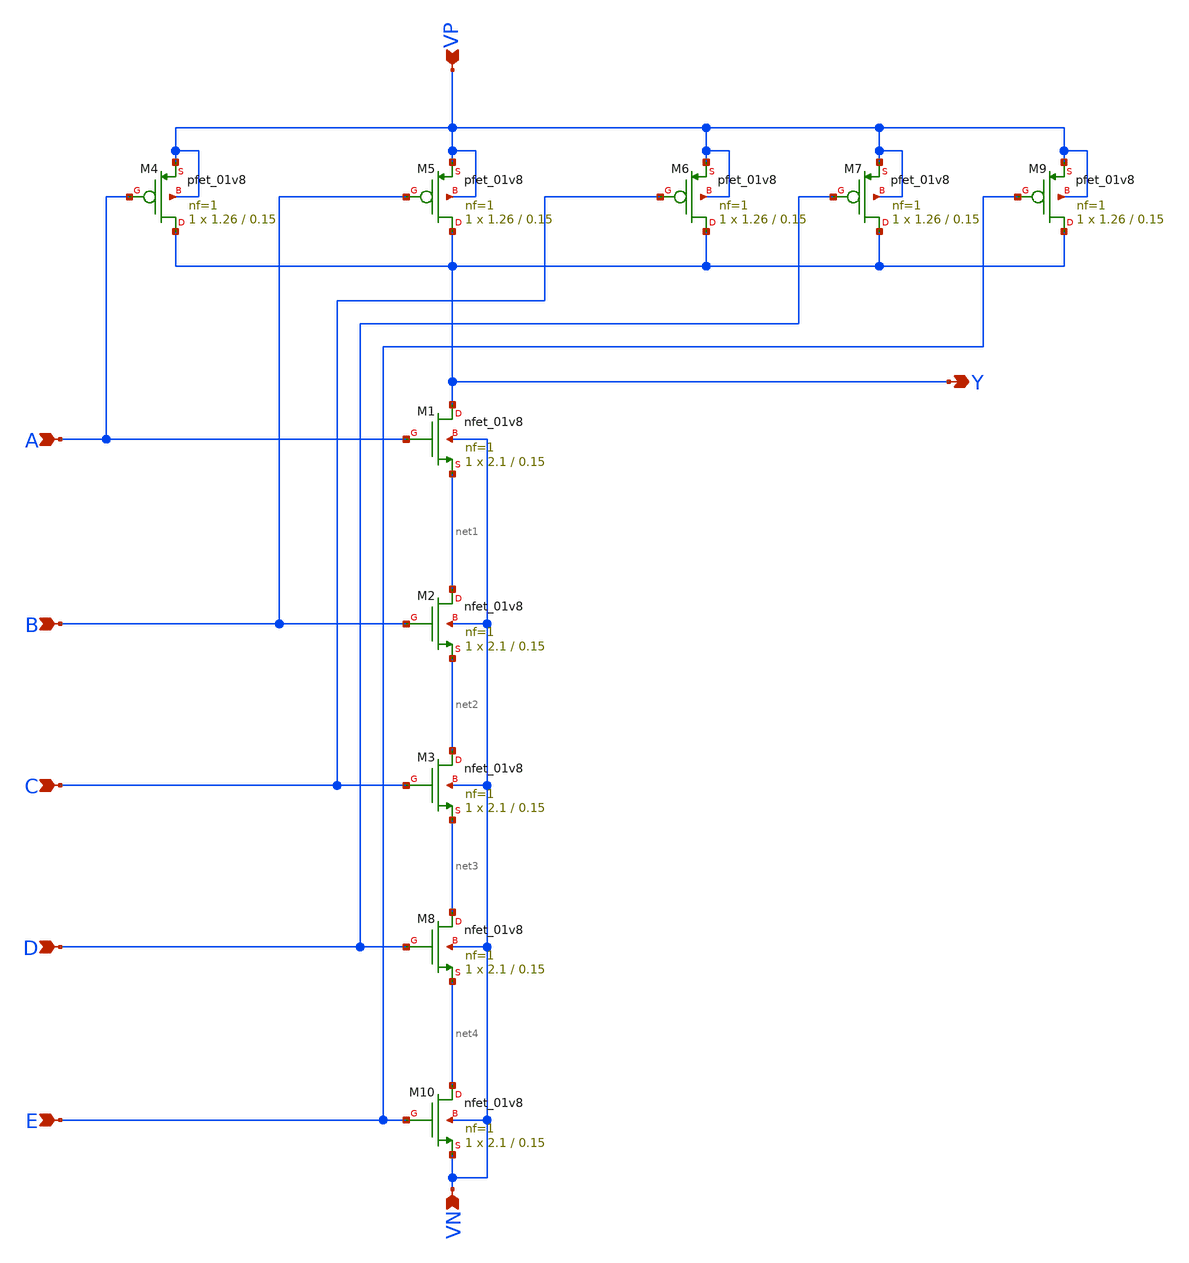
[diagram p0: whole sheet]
** sch_path: component/NAND5/nand5.sch
**.subckt nand5 A B C Y D E VN VP
*.ipin A
*.ipin B
*.ipin C
*.opin Y
*.ipin D
*.ipin E
*.ipin VN
*.ipin VP
XM1 Y A net1 VN sky130_fd_pr__nfet_01v8 L=0.15 W=2.1 nf=1 ad='int((nf+1)/2) * W/nf * 0.29' as='int((nf+2)/2) * W/nf * 0.29'
+ pd='2*int((nf+1)/2) * (W/nf + 0.29)' ps='2*int((nf+2)/2) * (W/nf + 0.29)' nrd='0.29 / W' nrs='0.29 / W'
+ sa=0 sb=0 sd=0 mult=1 m=1
XM2 net1 B net2 VN sky130_fd_pr__nfet_01v8 L=0.15 W=2.1 nf=1 ad='int((nf+1)/2) * W/nf * 0.29' as='int((nf+2)/2) * W/nf * 0.29'
+ pd='2*int((nf+1)/2) * (W/nf + 0.29)' ps='2*int((nf+2)/2) * (W/nf + 0.29)' nrd='0.29 / W' nrs='0.29 / W'
+ sa=0 sb=0 sd=0 mult=1 m=1
XM3 net2 C net3 VN sky130_fd_pr__nfet_01v8 L=0.15 W=2.1 nf=1 ad='int((nf+1)/2) * W/nf * 0.29' as='int((nf+2)/2) * W/nf * 0.29'
+ pd='2*int((nf+1)/2) * (W/nf + 0.29)' ps='2*int((nf+2)/2) * (W/nf + 0.29)' nrd='0.29 / W' nrs='0.29 / W'
+ sa=0 sb=0 sd=0 mult=1 m=1
XM4 Y A VP VP sky130_fd_pr__pfet_01v8 L=0.15 W=1.26 nf=1 ad='int((nf+1)/2) * W/nf * 0.29' as='int((nf+2)/2) * W/nf * 0.29'
+ pd='2*int((nf+1)/2) * (W/nf + 0.29)' ps='2*int((nf+2)/2) * (W/nf + 0.29)' nrd='0.29 / W' nrs='0.29 / W'
+ sa=0 sb=0 sd=0 mult=1 m=1
XM5 Y B VP VP sky130_fd_pr__pfet_01v8 L=0.15 W=1.26 nf=1 ad='int((nf+1)/2) * W/nf * 0.29' as='int((nf+2)/2) * W/nf * 0.29'
+ pd='2*int((nf+1)/2) * (W/nf + 0.29)' ps='2*int((nf+2)/2) * (W/nf + 0.29)' nrd='0.29 / W' nrs='0.29 / W'
+ sa=0 sb=0 sd=0 mult=1 m=1
XM6 Y C VP VP sky130_fd_pr__pfet_01v8 L=0.15 W=1.26 nf=1 ad='int((nf+1)/2) * W/nf * 0.29' as='int((nf+2)/2) * W/nf * 0.29'
+ pd='2*int((nf+1)/2) * (W/nf + 0.29)' ps='2*int((nf+2)/2) * (W/nf + 0.29)' nrd='0.29 / W' nrs='0.29 / W'
+ sa=0 sb=0 sd=0 mult=1 m=1
XM7 Y D VP VP sky130_fd_pr__pfet_01v8 L=0.15 W=1.26 nf=1 ad='int((nf+1)/2) * W/nf * 0.29' as='int((nf+2)/2) * W/nf * 0.29'
+ pd='2*int((nf+1)/2) * (W/nf + 0.29)' ps='2*int((nf+2)/2) * (W/nf + 0.29)' nrd='0.29 / W' nrs='0.29 / W'
+ sa=0 sb=0 sd=0 mult=1 m=1
XM8 net3 D net4 VN sky130_fd_pr__nfet_01v8 L=0.15 W=2.1 nf=1 ad='int((nf+1)/2) * W/nf * 0.29' as='int((nf+2)/2) * W/nf * 0.29'
+ pd='2*int((nf+1)/2) * (W/nf + 0.29)' ps='2*int((nf+2)/2) * (W/nf + 0.29)' nrd='0.29 / W' nrs='0.29 / W'
+ sa=0 sb=0 sd=0 mult=1 m=1
XM9 Y E VP VP sky130_fd_pr__pfet_01v8 L=0.15 W=1.26 nf=1 ad='int((nf+1)/2) * W/nf * 0.29' as='int((nf+2)/2) * W/nf * 0.29'
+ pd='2*int((nf+1)/2) * (W/nf + 0.29)' ps='2*int((nf+2)/2) * (W/nf + 0.29)' nrd='0.29 / W' nrs='0.29 / W'
+ sa=0 sb=0 sd=0 mult=1 m=1
XM10 net4 E VN VN sky130_fd_pr__nfet_01v8 L=0.15 W=2.1 nf=1 ad='int((nf+1)/2) * W/nf * 0.29' as='int((nf+2)/2) * W/nf * 0.29'
+ pd='2*int((nf+1)/2) * (W/nf + 0.29)' ps='2*int((nf+2)/2) * (W/nf + 0.29)' nrd='0.29 / W' nrs='0.29 / W'
+ sa=0 sb=0 sd=0 mult=1 m=1
**.ends
.end
